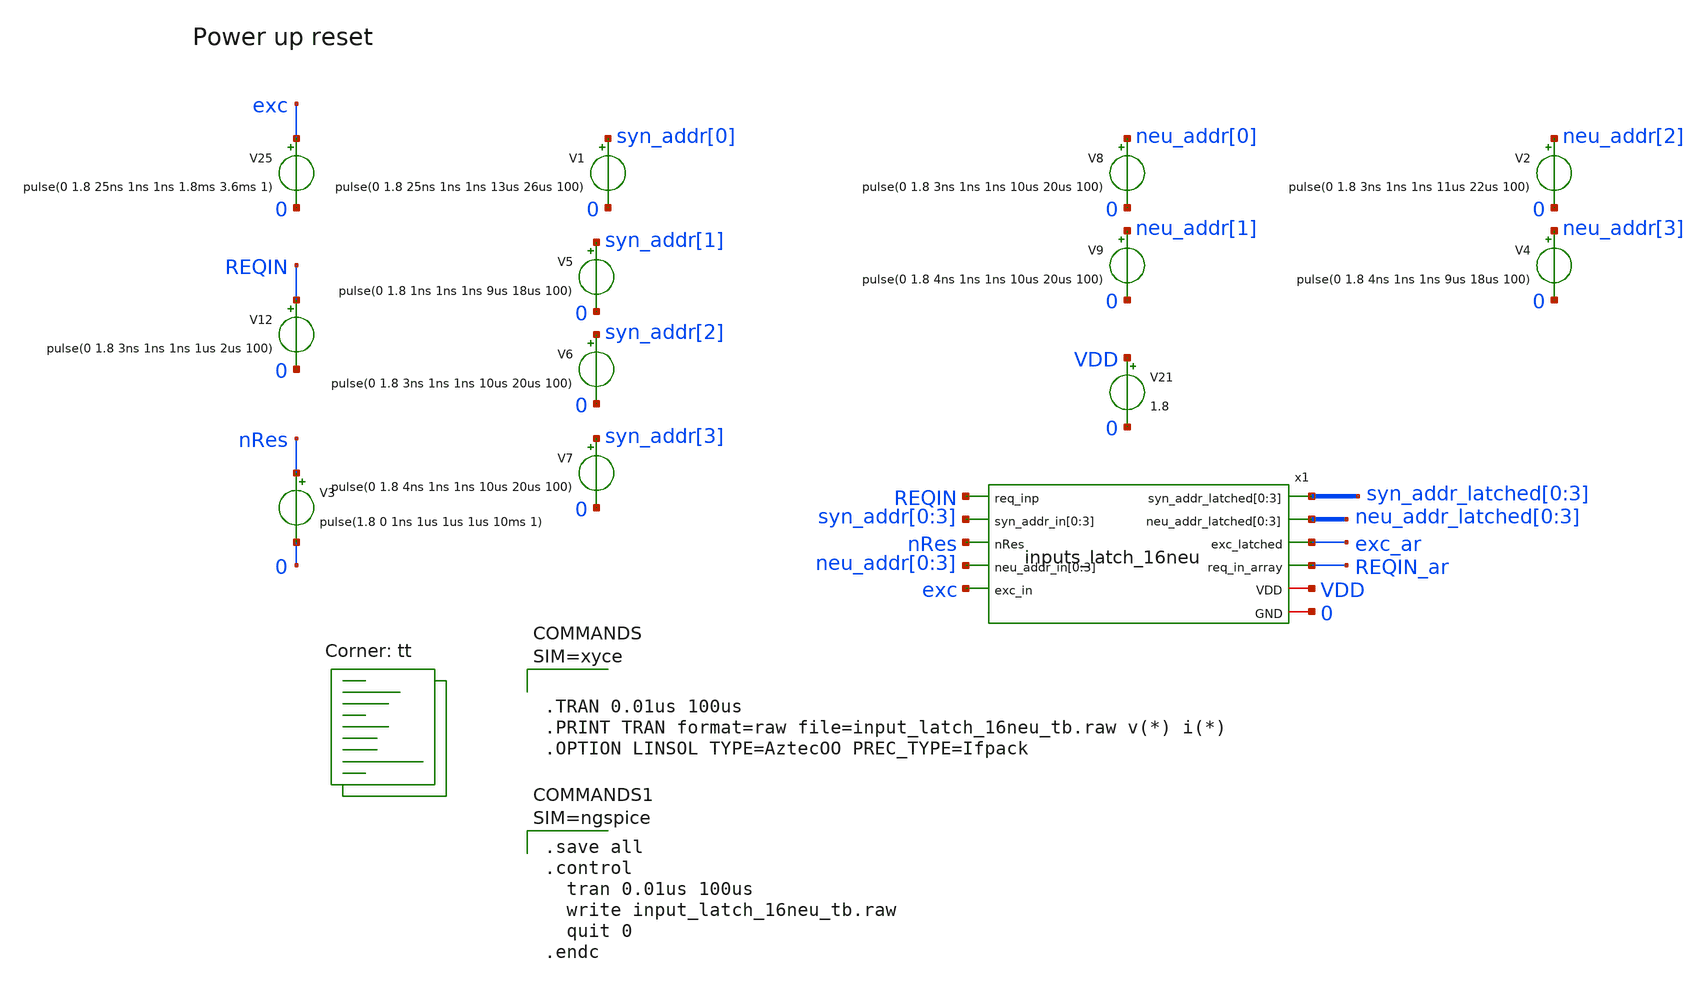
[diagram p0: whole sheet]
** sch_path: design/xschem/input_latch_16neu_tb.sch
**.subckt input_latch_16neu_tb
V12 REQIN 0 pulse(0 1.8 3ns 1ns 1ns 1us 2us 100)
V21 VDD 0 1.8
V25 exc 0 pulse(0 1.8 25ns 1ns 1ns 1.8ms 3.6ms 1)
V3 nRes 0 pulse(1.8 0 1ns 1us 1us 1us 10ms 1)
V1 syn_addr[0] 0 pulse(0 1.8 25ns 1ns 1ns 13us 26us 100)
V5 syn_addr[1] 0 pulse(0 1.8 1ns 1ns 1ns 9us 18us 100)
V6 syn_addr[2] 0 pulse(0 1.8 3ns 1ns 1ns 10us 20us 100)
V7 syn_addr[3] 0 pulse(0 1.8 4ns 1ns 1ns 10us 20us 100)
V8 neu_addr[0] 0 pulse(0 1.8 3ns 1ns 1ns 10us 20us 100)
V9 neu_addr[1] 0 pulse(0 1.8 4ns 1ns 1ns 10us 20us 100)
V2 neu_addr[2] 0 pulse(0 1.8 3ns 1ns 1ns 11us 22us 100)
V4 neu_addr[3] 0 pulse(0 1.8 4ns 1ns 1ns 9us 18us 100)
x1 REQIN syn_addr_latched[0] syn_addr_latched[1] syn_addr_latched[2] syn_addr_latched[3] syn_addr[0]
+ syn_addr[1] syn_addr[2] syn_addr[3] nRes neu_addr_latched[0] neu_addr_latched[1] neu_addr_latched[2]
+ neu_addr_latched[3] neu_addr[0] neu_addr[1] neu_addr[2] neu_addr[3] exc_ar exc REQIN_ar VDD 0 inputs_latch_16neu
**** begin user architecture code


* Standard cell simulation files
.include $::SKYWATER_STDCELLS/sky130_fd_sc_hd.spice


.lib $::SKYWATER_MODELS/sky130.lib.spice tt





.save all
.control
  tran 0.01us 100us
  write input_latch_16neu_tb.raw
  quit 0
.endc



**** end user architecture code
**.ends

* expanding   symbol:  inputs_latch_16neu.sym # of pins=11
** sym_path: design/xschem/inputs_latch_16neu.sym
** sch_path: design/xschem/inputs_latch_16neu.sch
.subckt inputs_latch_16neu req_inp syn_addr_latched[0] syn_addr_latched[1] syn_addr_latched[2]
+ syn_addr_latched[3] syn_addr_in[0] syn_addr_in[1] syn_addr_in[2] syn_addr_in[3] nRes neu_addr_latched[0]
+ neu_addr_latched[1] neu_addr_latched[2] neu_addr_latched[3] neu_addr_in[0] neu_addr_in[1] neu_addr_in[2] neu_addr_in[3]
+ exc_latched exc_in req_in_array VDD GND
*.ipin neu_addr_in[0],neu_addr_in[1],neu_addr_in[2],neu_addr_in[3]
*.ipin req_inp
*.ipin syn_addr_in[0],syn_addr_in[1],syn_addr_in[2],syn_addr_in[3]
*.ipin exc_in
*.ipin nRes
*.opin syn_addr_latched[0],syn_addr_latched[1],syn_addr_latched[2],syn_addr_latched[3]
*.opin neu_addr_latched[0],neu_addr_latched[1],neu_addr_latched[2],neu_addr_latched[3]
*.opin exc_latched
*.opin req_in_array
*.iopin VDD
*.iopin GND
x2[0] req_inp syn_addr_in[0] nRes GND GND VDD VDD syn_addr_latched[0] sky130_fd_sc_hd__dfrtp_1
x2[1] req_inp syn_addr_in[1] nRes GND GND VDD VDD syn_addr_latched[1] sky130_fd_sc_hd__dfrtp_1
x2[2] req_inp syn_addr_in[2] nRes GND GND VDD VDD syn_addr_latched[2] sky130_fd_sc_hd__dfrtp_1
x2[3] req_inp syn_addr_in[3] nRes GND GND VDD VDD syn_addr_latched[3] sky130_fd_sc_hd__dfrtp_1
x1[0] req_inp neu_addr_in[0] nRes GND GND VDD VDD neu_addr_latched[0] sky130_fd_sc_hd__dfrtp_1
x1[1] req_inp neu_addr_in[1] nRes GND GND VDD VDD neu_addr_latched[1] sky130_fd_sc_hd__dfrtp_1
x1[2] req_inp neu_addr_in[2] nRes GND GND VDD VDD neu_addr_latched[2] sky130_fd_sc_hd__dfrtp_1
x1[3] req_inp neu_addr_in[3] nRes GND GND VDD VDD neu_addr_latched[3] sky130_fd_sc_hd__dfrtp_1
x3 req_inp exc_in nRes GND GND VDD VDD exc_latched sky130_fd_sc_hd__dfrtp_1
x7 req_inp GND GND VDD VDD net1 sky130_fd_sc_hd__inv_1
x1 net1 GND GND VDD VDD net2 sky130_fd_sc_hd__inv_1
x2 net2 GND GND VDD VDD net3 sky130_fd_sc_hd__inv_1
x4 net3 GND GND VDD VDD req_in_array sky130_fd_sc_hd__inv_1
.ends

.end
